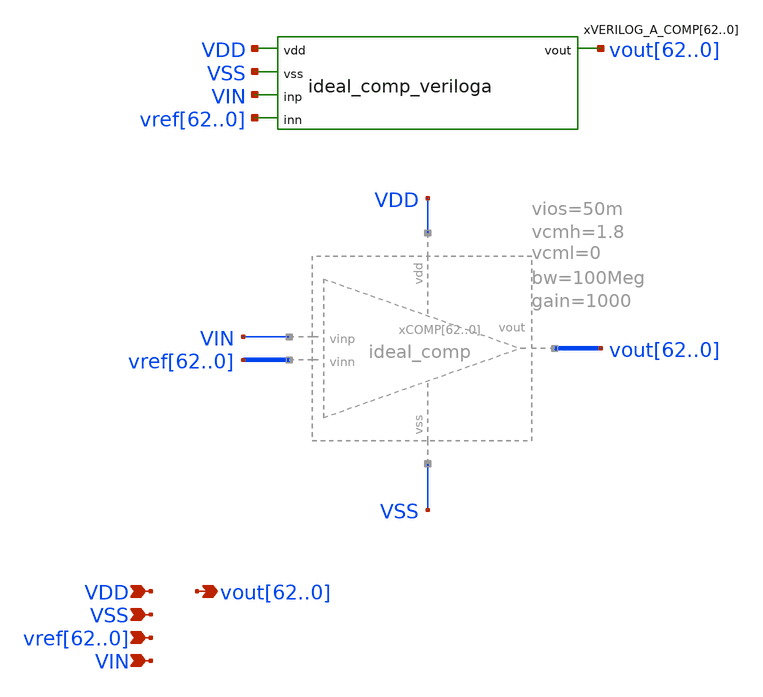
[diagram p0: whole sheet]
** sch_path: schematics/comp_top_ideal.sch
**.subckt comp_top_ideal
*+ vout62,vout61,vout60,vout59,vout58,vout57,vout56,vout55,vout54,vout53,vout52,vout51,vout50,vout49,vout48,vout47,vout46,vout45,vout44,vout43,vout42,vout41,vout40,vout39,vout38,vout37,vout36,vout35,vout34,vout33,vout32,vout31,vout30,vout29,vout28,vout27,vout26,vout25,vout24,vout23,vout22,vout21,vout20,vout19,vout18,vout17,vout16,vout15,vout14,vout13,vout12,vout11,vout10,vout9,vout8,vout7,vout6,vout5,vout4,vout3,vout2,vout1,vout0 VDD VSS
*+ vref62,vref61,vref60,vref59,vref58,vref57,vref56,vref55,vref54,vref53,vref52,vref51,vref50,vref49,vref48,vref47,vref46,vref45,vref44,vref43,vref42,vref41,vref40,vref39,vref38,vref37,vref36,vref35,vref34,vref33,vref32,vref31,vref30,vref29,vref28,vref27,vref26,vref25,vref24,vref23,vref22,vref21,vref20,vref19,vref18,vref17,vref16,vref15,vref14,vref13,vref12,vref11,vref10,vref9,vref8,vref7,vref6,vref5,vref4,vref3,vref2,vref1,vref0 VIN
*.opin
*+ vout62,vout61,vout60,vout59,vout58,vout57,vout56,vout55,vout54,vout53,vout52,vout51,vout50,vout49,vout48,vout47,vout46,vout45,vout44,vout43,vout42,vout41,vout40,vout39,vout38,vout37,vout36,vout35,vout34,vout33,vout32,vout31,vout30,vout29,vout28,vout27,vout26,vout25,vout24,vout23,vout22,vout21,vout20,vout19,vout18,vout17,vout16,vout15,vout14,vout13,vout12,vout11,vout10,vout9,vout8,vout7,vout6,vout5,vout4,vout3,vout2,vout1,vout0
*.ipin VDD
*.ipin VSS
*.ipin
*+ vref62,vref61,vref60,vref59,vref58,vref57,vref56,vref55,vref54,vref53,vref52,vref51,vref50,vref49,vref48,vref47,vref46,vref45,vref44,vref43,vref42,vref41,vref40,vref39,vref38,vref37,vref36,vref35,vref34,vref33,vref32,vref31,vref30,vref29,vref28,vref27,vref26,vref25,vref24,vref23,vref22,vref21,vref20,vref19,vref18,vref17,vref16,vref15,vref14,vref13,vref12,vref11,vref10,vref9,vref8,vref7,vref6,vref5,vref4,vref3,vref2,vref1,vref0
*.ipin VIN
xVERILOG_A_COMP62 VDD VSS VIN vref62 vout62 ideal_comp_cell
xVERILOG_A_COMP61 VDD VSS VIN vref61 vout61 ideal_comp_cell
xVERILOG_A_COMP60 VDD VSS VIN vref60 vout60 ideal_comp_cell
xVERILOG_A_COMP59 VDD VSS VIN vref59 vout59 ideal_comp_cell
xVERILOG_A_COMP58 VDD VSS VIN vref58 vout58 ideal_comp_cell
xVERILOG_A_COMP57 VDD VSS VIN vref57 vout57 ideal_comp_cell
xVERILOG_A_COMP56 VDD VSS VIN vref56 vout56 ideal_comp_cell
xVERILOG_A_COMP55 VDD VSS VIN vref55 vout55 ideal_comp_cell
xVERILOG_A_COMP54 VDD VSS VIN vref54 vout54 ideal_comp_cell
xVERILOG_A_COMP53 VDD VSS VIN vref53 vout53 ideal_comp_cell
xVERILOG_A_COMP52 VDD VSS VIN vref52 vout52 ideal_comp_cell
xVERILOG_A_COMP51 VDD VSS VIN vref51 vout51 ideal_comp_cell
xVERILOG_A_COMP50 VDD VSS VIN vref50 vout50 ideal_comp_cell
xVERILOG_A_COMP49 VDD VSS VIN vref49 vout49 ideal_comp_cell
xVERILOG_A_COMP48 VDD VSS VIN vref48 vout48 ideal_comp_cell
xVERILOG_A_COMP47 VDD VSS VIN vref47 vout47 ideal_comp_cell
xVERILOG_A_COMP46 VDD VSS VIN vref46 vout46 ideal_comp_cell
xVERILOG_A_COMP45 VDD VSS VIN vref45 vout45 ideal_comp_cell
xVERILOG_A_COMP44 VDD VSS VIN vref44 vout44 ideal_comp_cell
xVERILOG_A_COMP43 VDD VSS VIN vref43 vout43 ideal_comp_cell
xVERILOG_A_COMP42 VDD VSS VIN vref42 vout42 ideal_comp_cell
xVERILOG_A_COMP41 VDD VSS VIN vref41 vout41 ideal_comp_cell
xVERILOG_A_COMP40 VDD VSS VIN vref40 vout40 ideal_comp_cell
xVERILOG_A_COMP39 VDD VSS VIN vref39 vout39 ideal_comp_cell
xVERILOG_A_COMP38 VDD VSS VIN vref38 vout38 ideal_comp_cell
xVERILOG_A_COMP37 VDD VSS VIN vref37 vout37 ideal_comp_cell
xVERILOG_A_COMP36 VDD VSS VIN vref36 vout36 ideal_comp_cell
xVERILOG_A_COMP35 VDD VSS VIN vref35 vout35 ideal_comp_cell
xVERILOG_A_COMP34 VDD VSS VIN vref34 vout34 ideal_comp_cell
xVERILOG_A_COMP33 VDD VSS VIN vref33 vout33 ideal_comp_cell
xVERILOG_A_COMP32 VDD VSS VIN vref32 vout32 ideal_comp_cell
xVERILOG_A_COMP31 VDD VSS VIN vref31 vout31 ideal_comp_cell
xVERILOG_A_COMP30 VDD VSS VIN vref30 vout30 ideal_comp_cell
xVERILOG_A_COMP29 VDD VSS VIN vref29 vout29 ideal_comp_cell
xVERILOG_A_COMP28 VDD VSS VIN vref28 vout28 ideal_comp_cell
xVERILOG_A_COMP27 VDD VSS VIN vref27 vout27 ideal_comp_cell
xVERILOG_A_COMP26 VDD VSS VIN vref26 vout26 ideal_comp_cell
xVERILOG_A_COMP25 VDD VSS VIN vref25 vout25 ideal_comp_cell
xVERILOG_A_COMP24 VDD VSS VIN vref24 vout24 ideal_comp_cell
xVERILOG_A_COMP23 VDD VSS VIN vref23 vout23 ideal_comp_cell
xVERILOG_A_COMP22 VDD VSS VIN vref22 vout22 ideal_comp_cell
xVERILOG_A_COMP21 VDD VSS VIN vref21 vout21 ideal_comp_cell
xVERILOG_A_COMP20 VDD VSS VIN vref20 vout20 ideal_comp_cell
xVERILOG_A_COMP19 VDD VSS VIN vref19 vout19 ideal_comp_cell
xVERILOG_A_COMP18 VDD VSS VIN vref18 vout18 ideal_comp_cell
xVERILOG_A_COMP17 VDD VSS VIN vref17 vout17 ideal_comp_cell
xVERILOG_A_COMP16 VDD VSS VIN vref16 vout16 ideal_comp_cell
xVERILOG_A_COMP15 VDD VSS VIN vref15 vout15 ideal_comp_cell
xVERILOG_A_COMP14 VDD VSS VIN vref14 vout14 ideal_comp_cell
xVERILOG_A_COMP13 VDD VSS VIN vref13 vout13 ideal_comp_cell
xVERILOG_A_COMP12 VDD VSS VIN vref12 vout12 ideal_comp_cell
xVERILOG_A_COMP11 VDD VSS VIN vref11 vout11 ideal_comp_cell
xVERILOG_A_COMP10 VDD VSS VIN vref10 vout10 ideal_comp_cell
xVERILOG_A_COMP9 VDD VSS VIN vref9 vout9 ideal_comp_cell
xVERILOG_A_COMP8 VDD VSS VIN vref8 vout8 ideal_comp_cell
xVERILOG_A_COMP7 VDD VSS VIN vref7 vout7 ideal_comp_cell
xVERILOG_A_COMP6 VDD VSS VIN vref6 vout6 ideal_comp_cell
xVERILOG_A_COMP5 VDD VSS VIN vref5 vout5 ideal_comp_cell
xVERILOG_A_COMP4 VDD VSS VIN vref4 vout4 ideal_comp_cell
xVERILOG_A_COMP3 VDD VSS VIN vref3 vout3 ideal_comp_cell
xVERILOG_A_COMP2 VDD VSS VIN vref2 vout2 ideal_comp_cell
xVERILOG_A_COMP1 VDD VSS VIN vref1 vout1 ideal_comp_cell
xVERILOG_A_COMP0 VDD VSS VIN vref0 vout0 ideal_comp_cell
**.ends

* expanding   symbol:  schematics/ideal_comp.sym # of pins=5
** sym_path: schematics/ideal_comp.sym
** sch_path: schematics/ideal_comp.sch
.subckt ideal_comp vdd vss vinp vout vinn  bw=100Meg gain=1000 vcmh=1.8 vcml=0 vios=50m
*.ipin vdd
*.opin vout
*.ipin vss
*.ipin vinp
*.ipin vinn
B1 vp vss V = {V(vinp)<vcmh ? (V(vinp) < vcml ? vcml: V(vinp)) : vcmh}
B2 vn vss V = {V(vinn)<vcmh ? (V(vinn) < vcml ? vcml: V(vinn) + vios) : vcmh}
B3 net1 vss V = {gain*(V(vp)-V(vn)) < V(vdd) ? (gain*(V(vp)-V(vn)) < V(vss) ? V(vss) : (gain*(V(vp)-V(vn)))) : V(vdd)}
R1 vout net1 {1/(2*3.1415*bw*1p)} m=1
C1 vout vss 1p m=1
.ends

**** begin user architecture code

.subckt ideal_comp_cell VDD VSS INP INN VOUT
N1 vdd vss inp inn vout ideal_comp_model
.ends ideal_comp_cell

.model ideal_comp_model ideal_comp


.control
* following line specifies the location for the .osdi file so ngspice can use it.
* working dir set in tcl in startup script as pwd in top location
pre_osdi $working_dir/schematics/verilog_a/ideal_comp.osdi
.endc

**** end user architecture code
.end
